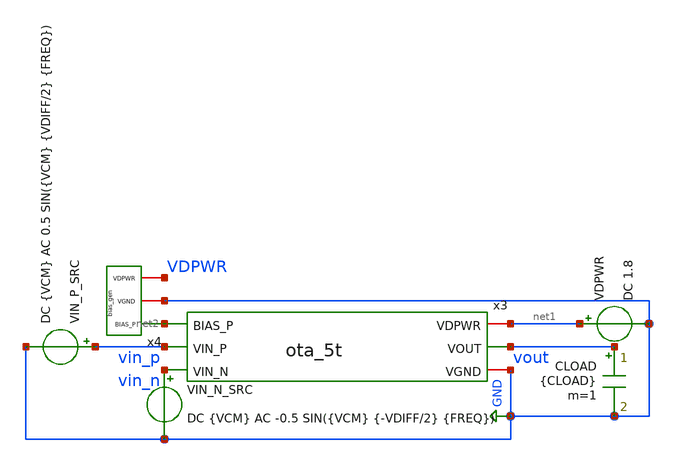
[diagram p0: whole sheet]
** sch_path: xschem-new/tb_ota_5t.sch
**.subckt tb_ota_5t
x3 net2 net1 vin_p vin_n vout GND ota_5t
x4 net2 GND VDPWR bias_gen
VIN_P_SRC vin_p GND DC {VCM} AC 0.5 SIN({VCM} {VDIFF/2} {FREQ})
VIN_N_SRC vin_n GND DC {VCM} AC -0.5 SIN({VCM} {-VDIFF/2} {FREQ})
VDPWR net1 GND DC 1.8
CLOAD vout GND {CLOAD} m=1
**** begin user architecture code


.lib /foss/pdks/sky130A/libs.tech/ngspice/sky130.lib.spice tt_mm

* =====================================================
* PARAMETERS
* =====================================================

.param VCM=0.9
.param VDIFF=100u
.param FREQ=10
.param CLOAD=1p

.option savecurrents

.control

* =====================================================
* DC OPERATING POINT
* =====================================================

op

print v(vout)
print v(vin_p)
print v(vin_n)

* =====================================================
* TRANSIENT ANALYSIS
* =====================================================

tran 100u 500m

plot v(vin_p) v(vin_n)
plot v(vout)

* =====================================================
* AC SMALL-SIGNAL ANALYSIS
* =====================================================

ac dec 100 1 1G

let vdiff = v(vin_p)-v(vin_n)

plot db(v(vout)/vdiff)
plot phase(v(vout)/vdiff)

.endc


**** end user architecture code
**.ends

* expanding   symbol:  ota_5t.sym # of pins=6
** sym_path: xschem-new/ota_5t.sym
** sch_path: xschem-new/ota_5t.sch
.subckt ota_5t BIAS_P VDPWR VIN_P VIN_N VOUT VGND
*.ipin VIN_P
*.ipin VIN_N
*.ipin BIAS_P
*.iopin VDPWR
*.iopin VGND
*.opin VOUT
XMDIFF_P net1 VIN_P TAIL_P VDPWR sky130_fd_pr__pfet_01v8 L=4 W=48 nf=1 ad='int((1 + 1)/2) * 48 / 1 * 0.29'
+ as='int((1 + 2)/2) * 48 / 1 * 0.29' pd='2*int((1 + 1)/2) * (48 / 1 + 0.29)' ps='2*int((1 + 2)/2) * (48 / 1 + 0.29)'
+ nrd='0.29 / 48 ' nrs='0.29 / 48 ' sa=0 sb=0 sd=0 mult=1 m=1
XMDIFF_N VOUT VIN_N TAIL_P VDPWR sky130_fd_pr__pfet_01v8 L=4 W=48 nf=1 ad='int((1 + 1)/2) * 48 / 1 * 0.29'
+ as='int((1 + 2)/2) * 48 / 1 * 0.29' pd='2*int((1 + 1)/2) * (48 / 1 + 0.29)' ps='2*int((1 + 2)/2) * (48 / 1 + 0.29)'
+ nrd='0.29 / 48 ' nrs='0.29 / 48 ' sa=0 sb=0 sd=0 mult=1 m=1
XMTAIL TAIL_P BIAS_P VDPWR VDPWR sky130_fd_pr__pfet_01v8 L=8 W=0.5 nf=1 ad='int((1 + 1)/2) * 0.5 / 1 * 0.29'
+ as='int((1 + 2)/2) * 0.5 / 1 * 0.29' pd='2*int((1 + 1)/2) * (0.5 / 1 + 0.29)' ps='2*int((1 + 2)/2) * (0.5 / 1 + 0.29)'
+ nrd='0.29 / 0.5 ' nrs='0.29 / 0.5 ' sa=0 sb=0 sd=0 mult=1 m=1
XMLOAD_REF net1 net1 VGND VGND sky130_fd_pr__nfet_01v8 L=16 W=8 nf=1 ad='int((1 + 1)/2) * 8 / 1 * 0.29'
+ as='int((1 + 2)/2) * 8 / 1 * 0.29' pd='2*int((1 + 1)/2) * (8 / 1 + 0.29)' ps='2*int((1 + 2)/2) * (8 / 1 + 0.29)'
+ nrd='0.29 / 8 ' nrs='0.29 / 8 ' sa=0 sb=0 sd=0 mult=1 m=1
XMLOAD_OUT VOUT net1 VGND VGND sky130_fd_pr__nfet_01v8 L=16 W=8 nf=1 ad='int((1 + 1)/2) * 8 / 1 * 0.29'
+ as='int((1 + 2)/2) * 8 / 1 * 0.29' pd='2*int((1 + 1)/2) * (8 / 1 + 0.29)' ps='2*int((1 + 2)/2) * (8 / 1 + 0.29)'
+ nrd='0.29 / 8 ' nrs='0.29 / 8 ' sa=0 sb=0 sd=0 mult=1 m=1
.ends


* expanding   symbol:  bias_gen.sym # of pins=3
** sym_path: xschem/bias_gen.sym
** sch_path: xschem/bias_gen.sch
.subckt bias_gen BIAS_P VGND VDPWR
*.iopin VDPWR
*.iopin VGND
*.opin BIAS_P
XM_BIAS_P BIAS_P BIAS_P VDPWR VDPWR sky130_fd_pr__pfet_01v8 L=2 W=1 nf=1 ad='int((1 + 1)/2) * 1 / 1 * 0.29'
+ as='int((1 + 2)/2) * 1 / 1 * 0.29' pd='2*int((1 + 1)/2) * (1 / 1 + 0.29)' ps='2*int((1 + 2)/2) * (1 / 1 + 0.29)'
+ nrd='0.29 / 1 ' nrs='0.29 / 1 ' sa=0 sb=0 sd=0 mult=1 m=1
XM_BIAS_N BIAS_P BIAS_P VGND VGND sky130_fd_pr__nfet_01v8 L=2 W=0.5 nf=1 ad='int((1 + 1)/2) * 0.5 / 1 * 0.29'
+ as='int((1 + 2)/2) * 0.5 / 1 * 0.29' pd='2*int((1 + 1)/2) * (0.5 / 1 + 0.29)' ps='2*int((1 + 2)/2) * (0.5 / 1 + 0.29)'
+ nrd='0.29 / 0.5 ' nrs='0.29 / 0.5 ' sa=0 sb=0 sd=0 mult=1 m=1
.ends

.GLOBAL GND
.end
